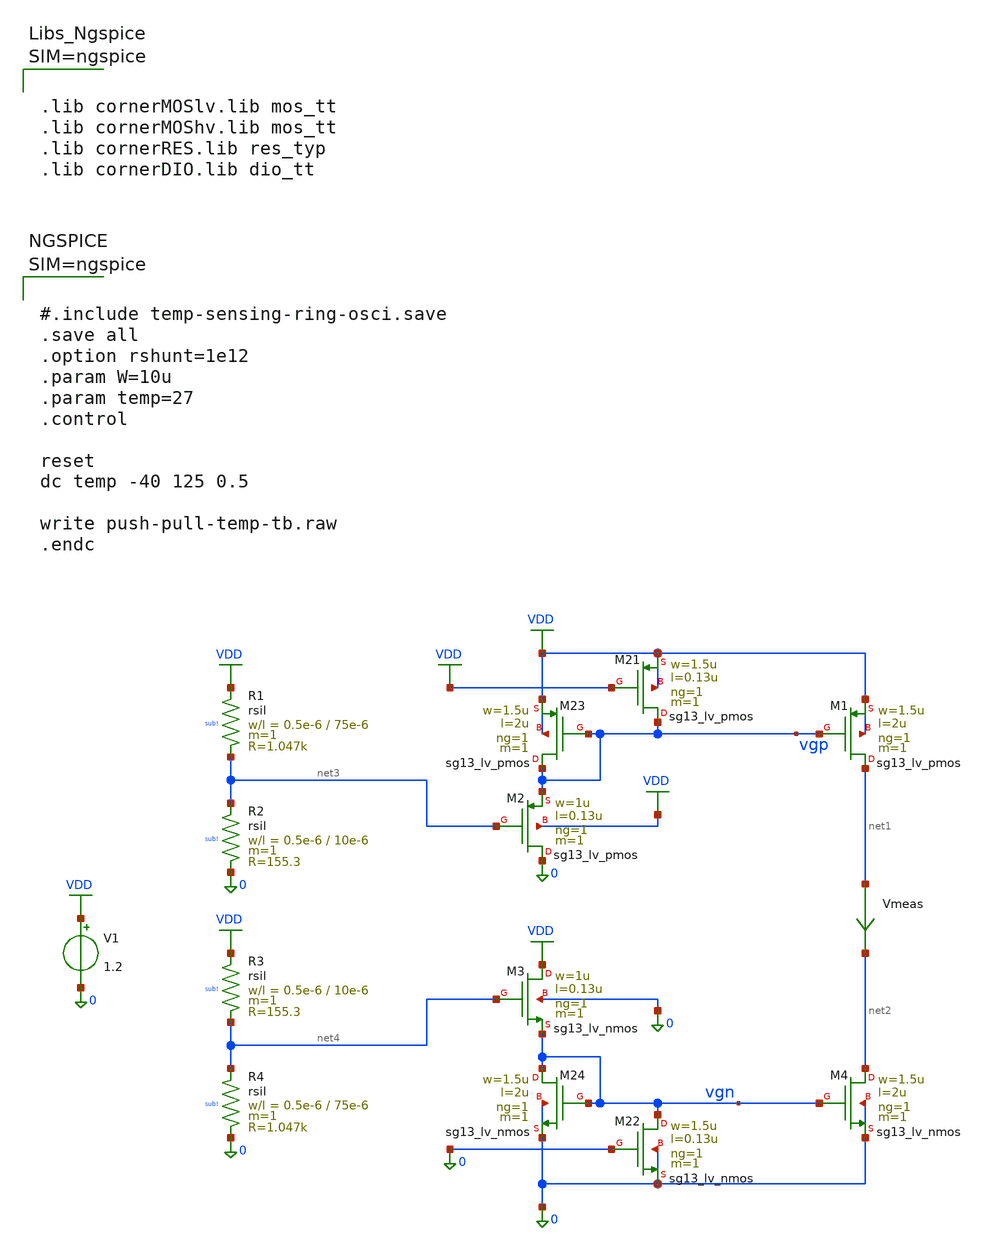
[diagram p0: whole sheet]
** sch_path: TSENSE8490-main/schematic/xschem/lvs-view/analog/temp-sens-core/testbenches/push-pull-tb/push-pull-tb.sch
**.subckt push-pull-tb
V1 VDD 0 1.2
XM1 net1 vgp VDD VDD sg13_lv_pmos w=1.5u l=2u ng=1 m=1 mm_ok=1
XM21 vgp VDD VDD VDD sg13_lv_pmos w=1.5u l=0.13u ng=1 m=1 mm_ok=1
XM22 vgn 0 0 0 sg13_lv_nmos w=1.5u l=0.13u ng=1 m=1 mm_ok=1
XM23 vgp vgp VDD VDD sg13_lv_pmos w=1.5u l=2u ng=1 m=1 mm_ok=1
XM24 vgn vgn 0 0 sg13_lv_nmos w=1.5u l=2u ng=1 m=1 mm_ok=1
XM4 net2 vgn 0 0 sg13_lv_nmos w=1.5u l=2u ng=1 m=1 mm_ok=1
Vmeas net1 net2 0
.save i(vmeas)
XR1 VDD net3 sub! rsil w=0.5e-6 l=75e-6 m=1 mm_ok=1
XR2 net3 0 sub! rsil w=0.5e-6 l=10e-6 m=1 mm_ok=1
XR4 net4 0 sub! rsil w=0.5e-6 l=75e-6 m=1 mm_ok=1
XR3 VDD net4 sub! rsil w=0.5e-6 l=10e-6 m=1 mm_ok=1
XM2 0 net3 vgp VDD sg13_lv_pmos w=1u l=0.13u ng=1 m=1 mm_ok=1
XM3 VDD net4 vgn 0 sg13_lv_nmos w=1u l=0.13u ng=1 m=1 mm_ok=1
**** begin user architecture code



.lib cornerMOSlv.lib mos_tt
.lib cornerMOShv.lib mos_tt
.lib cornerRES.lib res_typ
.lib cornerDIO.lib dio_tt






#.include temp-sensing-ring-osci.save
.save all
.option rshunt=1e12
.param W=10u
.param temp=27
.control

reset
dc temp -40 125 0.5

write push-pull-temp-tb.raw
.endc



**** end user architecture code
**.ends
.GLOBAL VDD
.end
